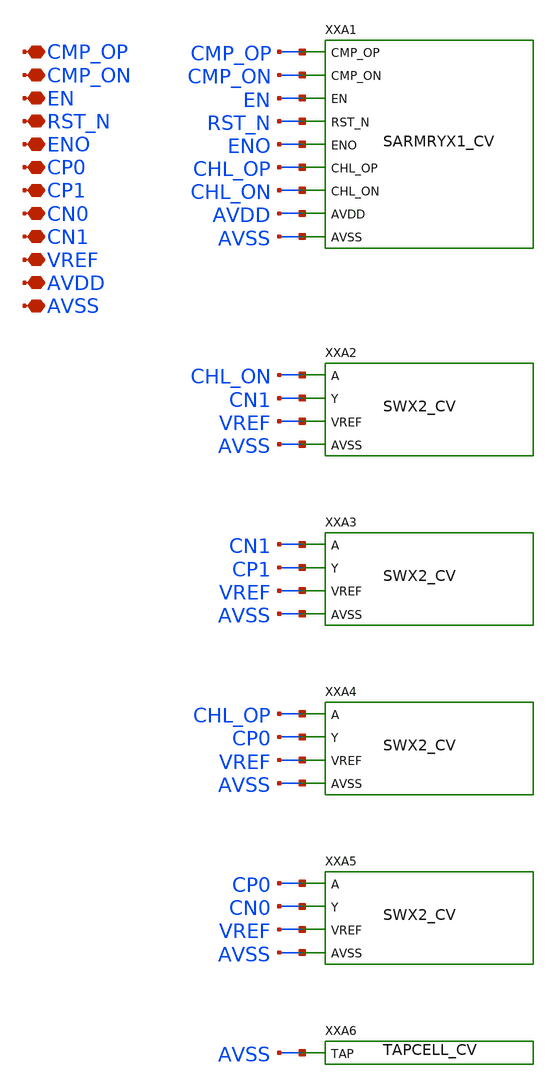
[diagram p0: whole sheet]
** sch_path: tests/transpile/SAR9B/SARDIGX1_CV.sch
**.subckt SARDIGX1_CV CMP_OP CMP_ON EN RST_N ENO CP0 CP1 CN0 CN1 VREF AVDD AVSS
*.iopin CMP_OP
*.iopin CMP_ON
*.iopin EN
*.iopin RST_N
*.iopin ENO
*.iopin CP0
*.iopin CP1
*.iopin CN0
*.iopin CN1
*.iopin VREF
*.iopin AVDD
*.iopin AVSS
XXA1 CMP_OP CMP_ON EN RST_N ENO CHL_OP CHL_ON AVDD AVSS SARMRYX1_CV
XXA2 CHL_ON CN1 VREF AVSS SWX2_CV
XXA3 CN1 CP1 VREF AVSS SWX2_CV
XXA4 CHL_OP CP0 VREF AVSS SWX2_CV
XXA5 CP0 CN0 VREF AVSS SWX2_CV
XXA6 AVSS TAPCELL_CV
**.ends
.end
